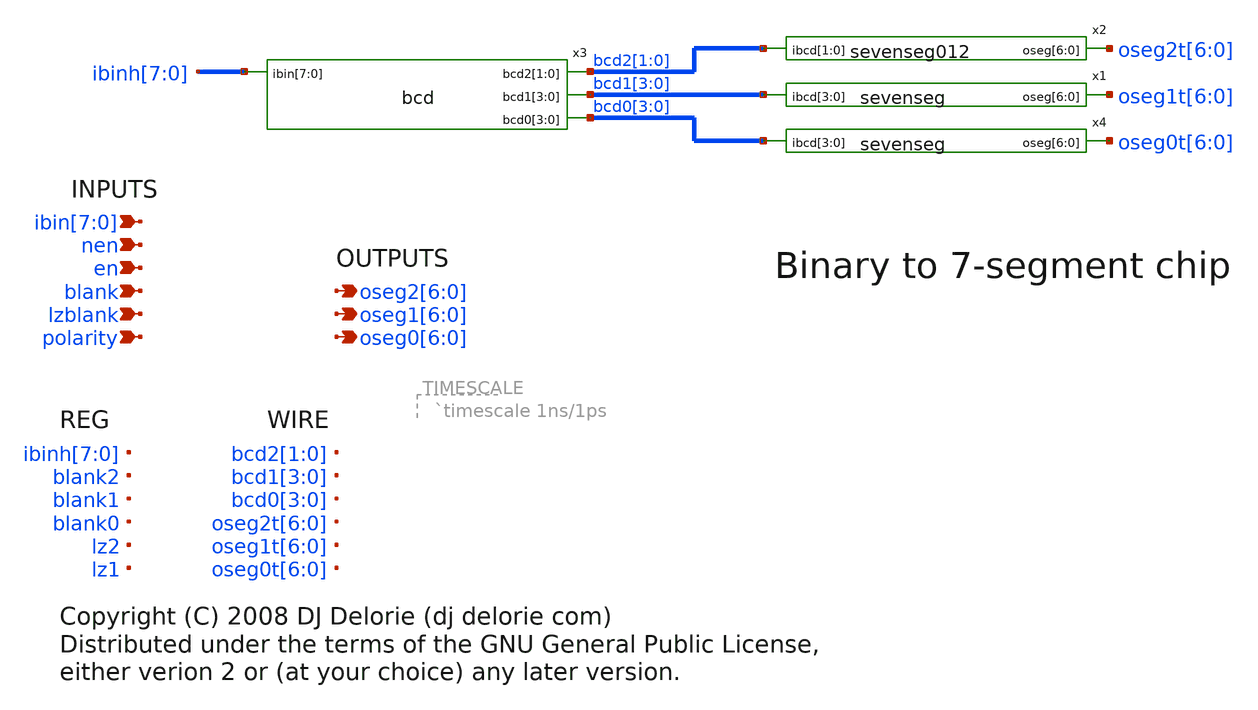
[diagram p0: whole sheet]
** sch_path: xschem-src/xschem_library/binto7seg/top.sch
* Copyright (C) 1998-2026 Stefan Frederik Schippers
* This program is free software; you can redistribute it and/or modify
* it under the terms of the GNU General Public License as published by
* the Free Software Foundation; either version 2 of the License, or
* (at your option) any later version.
* This program is distributed in the hope that it will be useful,
* but WITHOUT ANY WARRANTY; without even the implied warranty of
* MERCHANTABILITY or FITNESS FOR A PARTICULAR PURPOSE.  See the
* GNU General Public License for more details.
* You should have received a copy of the GNU General Public License
* along with this program; if not, write to the Free Software
* xschem-src/xschem_library/binto7seg/bcd.sch:
* C {code.sym} 260 -380 0 0 {name=CODE value="// Copyright (C) 2008 DJ Delorie <dj delorie com>
**.subckt top nen en blank polarity lzblank
*+ ibin[7],ibin[6],ibin[5],ibin[4],ibin[3],ibin[2],ibin[1],ibin[0] oseg2[6],oseg2[5],oseg2[4],oseg2[3],oseg2[2],oseg2[1],oseg2[0]
*+ oseg1[6],oseg1[5],oseg1[4],oseg1[3],oseg1[2],oseg1[1],oseg1[0] oseg0[6],oseg0[5],oseg0[4],oseg0[3],oseg0[2],oseg0[1],oseg0[0]
*.ipin nen
*.ipin en
*.ipin blank
*.ipin polarity
*.ipin lzblank
*.ipin ibin[7],ibin[6],ibin[5],ibin[4],ibin[3],ibin[2],ibin[1],ibin[0]
*.opin oseg2[6],oseg2[5],oseg2[4],oseg2[3],oseg2[2],oseg2[1],oseg2[0]
*.opin oseg1[6],oseg1[5],oseg1[4],oseg1[3],oseg1[2],oseg1[1],oseg1[0]
*.opin oseg0[6],oseg0[5],oseg0[4],oseg0[3],oseg0[2],oseg0[1],oseg0[0]
x1 oseg1t[6] oseg1t[5] oseg1t[4] oseg1t[3] oseg1t[2] oseg1t[1] oseg1t[0] bcd1[3] bcd1[2] bcd1[1]
+ bcd1[0] sevenseg
x2 oseg2t[6] oseg2t[5] oseg2t[4] oseg2t[3] oseg2t[2] oseg2t[1] oseg2t[0] bcd2[1] bcd2[0] sevenseg012
x3 bcd2[1] bcd2[0] ibinh[7] ibinh[6] ibinh[5] ibinh[4] ibinh[3] ibinh[2] ibinh[1] ibinh[0] bcd1[3]
+ bcd1[2] bcd1[1] bcd1[0] bcd0[3] bcd0[2] bcd0[1] bcd0[0] bcd
x4 oseg0t[6] oseg0t[5] oseg0t[4] oseg0t[3] oseg0t[2] oseg0t[1] oseg0t[0] bcd0[3] bcd0[2] bcd0[1]
+ bcd0[0] sevenseg
**** begin user architecture code

// Copyright (C) 2008 DJ Delorie <dj delorie com>
// Distributed under the terms of the GNU General Public License,
// either verion 2 or (at your choice) any later version.

always @ (ibin, nen, en)
begin
  if (en & ~ nen)
    ibinh = ibin;
  else
    ibinh = ibinh;
end


always @ (bcd2, bcd1)
begin
  lz2 = (bcd2 == 0) ? 1 : 0;
  lz1 = (bcd1 == 0) ? lz2 : 0;
end

always @ (lz2, lz1, lzblank, blank)
begin
  blank2 = (lzblank & lz2) | blank;
  blank1 = (lzblank & lz1) | blank;
  blank0 = blank;
end

always @ (oseg2t, polarity, blank2)
begin
  if (blank2)
    oseg2 = 7'bZ;
  else if (polarity)
    oseg2 = ~ oseg2t;
  else
    oseg2 = oseg2t;
end

always @ (oseg1t, polarity, blank1, blank2)
begin
  if (blank1)
    oseg1 = 7'bZ;
  else if (polarity)
    oseg1 = ~ oseg1t;
  else
    oseg1 = oseg1t;
end

always @ (oseg0t, polarity, blank0)
begin
  if (blank0)
    oseg0 = 7'bZ;
  else if (polarity)
    oseg0 = ~ oseg0t;
  else
    oseg0 = oseg0t;
end




reg [7:0] iibin;
reg ien;
reg inen;
reg iblank;
reg ilzblank;
reg ipolarity;

initial begin
  $dumpfile("dumpfile.vcd");
  $dumpvars(0, top);
end

task binpattern;
begin
  iibin = 0;
  #100;
  iibin = 1;
  #100;
  iibin = 2;
  #100;
  iibin = 234;
  #100;
  iibin = 255;
  #100;
  iibin = 188;
  #100;
  iibin = 222;
  #100;
end endtask

initial begin
  ien = 1;
  inen = 0;
  iblank = 0;
  ilzblank = 0;
  ipolarity = 0;
  binpattern;
  ilzblank = 1; // blank leading zeros
  binpattern;
end

assign en = ien;
assign nen = inen;
assign ibin = iibin;
assign blank = iblank;
assign lzblank = ilzblank;
assign polarity = ipolarity;


**** end user architecture code
**.ends

* expanding   symbol:  sevenseg.sym # of pins=2
** sym_path: xschem-src/xschem_library/binto7seg/sevenseg.sym
** sch_path: xschem-src/xschem_library/binto7seg/sevenseg.sch
.subckt sevenseg oseg[6] oseg[5] oseg[4] oseg[3] oseg[2] oseg[1] oseg[0] ibcd[3] ibcd[2] ibcd[1] ibcd[0]
*.ipin ibcd[3],ibcd[2],ibcd[1],ibcd[0]
*.opin oseg[6],oseg[5],oseg[4],oseg[3],oseg[2],oseg[1],oseg[0]
**** begin user architecture code

// Copyright (C) 2008 DJ Delorie <dj delorie com>
// Distributed under the terms of the GNU General Public License,
// either verion 2 or (at your choice) any later version.

always @ (ibcd)
begin
  case (ibcd)  // abcdefg
    0 : oseg = 7'b1111110;
    1 : oseg = 7'b0110000;
    2 : oseg = 7'b1101101;
    3 : oseg = 7'b1111001;
    4 : oseg = 7'b0110011;
    5 : oseg = 7'b1011011;
    6 : oseg = 7'b1011111;
    7 : oseg = 7'b1110000;
    8 : oseg = 7'b1111111;
    9 : oseg = 7'b1111011;
    default : oseg = 0;
  endcase
end



**** end user architecture code
.ends


* expanding   symbol:  sevenseg012.sym # of pins=2
** sym_path: xschem-src/xschem_library/binto7seg/sevenseg012.sym
** sch_path: xschem-src/xschem_library/binto7seg/sevenseg012.sch
.subckt sevenseg012 oseg[6] oseg[5] oseg[4] oseg[3] oseg[2] oseg[1] oseg[0] ibcd[1] ibcd[0]
*.ipin ibcd[1],ibcd[0]
*.opin oseg[6],oseg[5],oseg[4],oseg[3],oseg[2],oseg[1],oseg[0]
**** begin user architecture code

// Copyright (C) 2008 DJ Delorie <dj delorie com>
// Distributed under the terms of the GNU General Public License,
// either verion 2 or (at your choice) any later version.

always @ (ibcd)
begin
  case (ibcd)  // abcdefg
    0 : oseg = 7'b1111110;
    1 : oseg = 7'b0110000;
    2 : oseg = 7'b1101101;
    default : oseg = 0;
  endcase
end


**** end user architecture code
.ends


* expanding   symbol:  bcd.sym # of pins=4
** sym_path: xschem-src/xschem_library/binto7seg/bcd.sym
** sch_path: xschem-src/xschem_library/binto7seg/bcd.sch
.subckt bcd bcd2[1] bcd2[0] ibin[7] ibin[6] ibin[5] ibin[4] ibin[3] ibin[2] ibin[1] ibin[0] bcd1[3]
+ bcd1[2] bcd1[1] bcd1[0] bcd0[3] bcd0[2] bcd0[1] bcd0[0]
*.ipin ibin[7],ibin[6],ibin[5],ibin[4],ibin[3],ibin[2],ibin[1],ibin[0]
*.opin bcd2[1],bcd2[0]
*.opin bcd1[3],bcd1[2],bcd1[1],bcd1[0]
*.opin bcd0[3],bcd0[2],bcd0[1],bcd0[0]
**** begin user architecture code

// Copyright (C) 2008 DJ Delorie <dj delorie com>
// Distributed under the terms of the GNU General Public License,
// either verion 2 or (at your choice) any later version.

always @ (ibin)
begin

  case (ibin)
    0 : begin bcd2 <= 2'b00; bcd1 <= 4'b0000; bcd0 <= 4'b0000; end
    1 : begin bcd2 <= 2'b00; bcd1 <= 4'b0000; bcd0 <= 4'b0001; end
    2 : begin bcd2 <= 2'b00; bcd1 <= 4'b0000; bcd0 <= 4'b0010; end
    3 : begin bcd2 <= 2'b00; bcd1 <= 4'b0000; bcd0 <= 4'b0011; end
    4 : begin bcd2 <= 2'b00; bcd1 <= 4'b0000; bcd0 <= 4'b0100; end
    5 : begin bcd2 <= 2'b00; bcd1 <= 4'b0000; bcd0 <= 4'b0101; end
    6 : begin bcd2 <= 2'b00; bcd1 <= 4'b0000; bcd0 <= 4'b0110; end
    7 : begin bcd2 <= 2'b00; bcd1 <= 4'b0000; bcd0 <= 4'b0111; end
    8 : begin bcd2 <= 2'b00; bcd1 <= 4'b0000; bcd0 <= 4'b1000; end
    9 : begin bcd2 <= 2'b00; bcd1 <= 4'b0000; bcd0 <= 4'b1001; end
    10 : begin bcd2 <= 2'b00; bcd1 <= 4'b0001; bcd0 <= 4'b0000; end
    11 : begin bcd2 <= 2'b00; bcd1 <= 4'b0001; bcd0 <= 4'b0001; end
    12 : begin bcd2 <= 2'b00; bcd1 <= 4'b0001; bcd0 <= 4'b0010; end
    13 : begin bcd2 <= 2'b00; bcd1 <= 4'b0001; bcd0 <= 4'b0011; end
    14 : begin bcd2 <= 2'b00; bcd1 <= 4'b0001; bcd0 <= 4'b0100; end
    15 : begin bcd2 <= 2'b00; bcd1 <= 4'b0001; bcd0 <= 4'b0101; end
    16 : begin bcd2 <= 2'b00; bcd1 <= 4'b0001; bcd0 <= 4'b0110; end
    17 : begin bcd2 <= 2'b00; bcd1 <= 4'b0001; bcd0 <= 4'b0111; end
    18 : begin bcd2 <= 2'b00; bcd1 <= 4'b0001; bcd0 <= 4'b1000; end
    19 : begin bcd2 <= 2'b00; bcd1 <= 4'b0001; bcd0 <= 4'b1001; end
    20 : begin bcd2 <= 2'b00; bcd1 <= 4'b0010; bcd0 <= 4'b0000; end
    21 : begin bcd2 <= 2'b00; bcd1 <= 4'b0010; bcd0 <= 4'b0001; end
    22 : begin bcd2 <= 2'b00; bcd1 <= 4'b0010; bcd0 <= 4'b0010; end
    23 : begin bcd2 <= 2'b00; bcd1 <= 4'b0010; bcd0 <= 4'b0011; end
    24 : begin bcd2 <= 2'b00; bcd1 <= 4'b0010; bcd0 <= 4'b0100; end
    25 : begin bcd2 <= 2'b00; bcd1 <= 4'b0010; bcd0 <= 4'b0101; end
    26 : begin bcd2 <= 2'b00; bcd1 <= 4'b0010; bcd0 <= 4'b0110; end
    27 : begin bcd2 <= 2'b00; bcd1 <= 4'b0010; bcd0 <= 4'b0111; end
    28 : begin bcd2 <= 2'b00; bcd1 <= 4'b0010; bcd0 <= 4'b1000; end
    29 : begin bcd2 <= 2'b00; bcd1 <= 4'b0010; bcd0 <= 4'b1001; end
    30 : begin bcd2 <= 2'b00; bcd1 <= 4'b0011; bcd0 <= 4'b0000; end
    31 : begin bcd2 <= 2'b00; bcd1 <= 4'b0011; bcd0 <= 4'b0001; end
    32 : begin bcd2 <= 2'b00; bcd1 <= 4'b0011; bcd0 <= 4'b0010; end
    33 : begin bcd2 <= 2'b00; bcd1 <= 4'b0011; bcd0 <= 4'b0011; end
    34 : begin bcd2 <= 2'b00; bcd1 <= 4'b0011; bcd0 <= 4'b0100; end
    35 : begin bcd2 <= 2'b00; bcd1 <= 4'b0011; bcd0 <= 4'b0101; end
    36 : begin bcd2 <= 2'b00; bcd1 <= 4'b0011; bcd0 <= 4'b0110; end
    37 : begin bcd2 <= 2'b00; bcd1 <= 4'b0011; bcd0 <= 4'b0111; end
    38 : begin bcd2 <= 2'b00; bcd1 <= 4'b0011; bcd0 <= 4'b1000; end
    39 : begin bcd2 <= 2'b00; bcd1 <= 4'b0011; bcd0 <= 4'b1001; end
    40 : begin bcd2 <= 2'b00; bcd1 <= 4'b0100; bcd0 <= 4'b0000; end
    41 : begin bcd2 <= 2'b00; bcd1 <= 4'b0100; bcd0 <= 4'b0001; end
    42 : begin bcd2 <= 2'b00; bcd1 <= 4'b0100; bcd0 <= 4'b0010; end
    43 : begin bcd2 <= 2'b00; bcd1 <= 4'b0100; bcd0 <= 4'b0011; end
    44 : begin bcd2 <= 2'b00; bcd1 <= 4'b0100; bcd0 <= 4'b0100; end
    45 : begin bcd2 <= 2'b00; bcd1 <= 4'b0100; bcd0 <= 4'b0101; end
    46 : begin bcd2 <= 2'b00; bcd1 <= 4'b0100; bcd0 <= 4'b0110; end
    47 : begin bcd2 <= 2'b00; bcd1 <= 4'b0100; bcd0 <= 4'b0111; end
    48 : begin bcd2 <= 2'b00; bcd1 <= 4'b0100; bcd0 <= 4'b1000; end
    49 : begin bcd2 <= 2'b00; bcd1 <= 4'b0100; bcd0 <= 4'b1001; end
    50 : begin bcd2 <= 2'b00; bcd1 <= 4'b0101; bcd0 <= 4'b0000; end
    51 : begin bcd2 <= 2'b00; bcd1 <= 4'b0101; bcd0 <= 4'b0001; end
    52 : begin bcd2 <= 2'b00; bcd1 <= 4'b0101; bcd0 <= 4'b0010; end
    53 : begin bcd2 <= 2'b00; bcd1 <= 4'b0101; bcd0 <= 4'b0011; end
    54 : begin bcd2 <= 2'b00; bcd1 <= 4'b0101; bcd0 <= 4'b0100; end
    55 : begin bcd2 <= 2'b00; bcd1 <= 4'b0101; bcd0 <= 4'b0101; end
    56 : begin bcd2 <= 2'b00; bcd1 <= 4'b0101; bcd0 <= 4'b0110; end
    57 : begin bcd2 <= 2'b00; bcd1 <= 4'b0101; bcd0 <= 4'b0111; end
    58 : begin bcd2 <= 2'b00; bcd1 <= 4'b0101; bcd0 <= 4'b1000; end
    59 : begin bcd2 <= 2'b00; bcd1 <= 4'b0101; bcd0 <= 4'b1001; end
    60 : begin bcd2 <= 2'b00; bcd1 <= 4'b0110; bcd0 <= 4'b0000; end
    61 : begin bcd2 <= 2'b00; bcd1 <= 4'b0110; bcd0 <= 4'b0001; end
    62 : begin bcd2 <= 2'b00; bcd1 <= 4'b0110; bcd0 <= 4'b0010; end
    63 : begin bcd2 <= 2'b00; bcd1 <= 4'b0110; bcd0 <= 4'b0011; end
    64 : begin bcd2 <= 2'b00; bcd1 <= 4'b0110; bcd0 <= 4'b0100; end
    65 : begin bcd2 <= 2'b00; bcd1 <= 4'b0110; bcd0 <= 4'b0101; end
    66 : begin bcd2 <= 2'b00; bcd1 <= 4'b0110; bcd0 <= 4'b0110; end
    67 : begin bcd2 <= 2'b00; bcd1 <= 4'b0110; bcd0 <= 4'b0111; end
    68 : begin bcd2 <= 2'b00; bcd1 <= 4'b0110; bcd0 <= 4'b1000; end
    69 : begin bcd2 <= 2'b00; bcd1 <= 4'b0110; bcd0 <= 4'b1001; end
    70 : begin bcd2 <= 2'b00; bcd1 <= 4'b0111; bcd0 <= 4'b0000; end
    71 : begin bcd2 <= 2'b00; bcd1 <= 4'b0111; bcd0 <= 4'b0001; end
    72 : begin bcd2 <= 2'b00; bcd1 <= 4'b0111; bcd0 <= 4'b0010; end
    73 : begin bcd2 <= 2'b00; bcd1 <= 4'b0111; bcd0 <= 4'b0011; end
    74 : begin bcd2 <= 2'b00; bcd1 <= 4'b0111; bcd0 <= 4'b0100; end
    75 : begin bcd2 <= 2'b00; bcd1 <= 4'b0111; bcd0 <= 4'b0101; end
    76 : begin bcd2 <= 2'b00; bcd1 <= 4'b0111; bcd0 <= 4'b0110; end
    77 : begin bcd2 <= 2'b00; bcd1 <= 4'b0111; bcd0 <= 4'b0111; end
    78 : begin bcd2 <= 2'b00; bcd1 <= 4'b0111; bcd0 <= 4'b1000; end
    79 : begin bcd2 <= 2'b00; bcd1 <= 4'b0111; bcd0 <= 4'b1001; end
    80 : begin bcd2 <= 2'b00; bcd1 <= 4'b1000; bcd0 <= 4'b0000; end
    81 : begin bcd2 <= 2'b00; bcd1 <= 4'b1000; bcd0 <= 4'b0001; end
    82 : begin bcd2 <= 2'b00; bcd1 <= 4'b1000; bcd0 <= 4'b0010; end
    83 : begin bcd2 <= 2'b00; bcd1 <= 4'b1000; bcd0 <= 4'b0011; end
    84 : begin bcd2 <= 2'b00; bcd1 <= 4'b1000; bcd0 <= 4'b0100; end
    85 : begin bcd2 <= 2'b00; bcd1 <= 4'b1000; bcd0 <= 4'b0101; end
    86 : begin bcd2 <= 2'b00; bcd1 <= 4'b1000; bcd0 <= 4'b0110; end
    87 : begin bcd2 <= 2'b00; bcd1 <= 4'b1000; bcd0 <= 4'b0111; end
    88 : begin bcd2 <= 2'b00; bcd1 <= 4'b1000; bcd0 <= 4'b1000; end
    89 : begin bcd2 <= 2'b00; bcd1 <= 4'b1000; bcd0 <= 4'b1001; end
    90 : begin bcd2 <= 2'b00; bcd1 <= 4'b1001; bcd0 <= 4'b0000; end
    91 : begin bcd2 <= 2'b00; bcd1 <= 4'b1001; bcd0 <= 4'b0001; end
    92 : begin bcd2 <= 2'b00; bcd1 <= 4'b1001; bcd0 <= 4'b0010; end
    93 : begin bcd2 <= 2'b00; bcd1 <= 4'b1001; bcd0 <= 4'b0011; end
    94 : begin bcd2 <= 2'b00; bcd1 <= 4'b1001; bcd0 <= 4'b0100; end
    95 : begin bcd2 <= 2'b00; bcd1 <= 4'b1001; bcd0 <= 4'b0101; end
    96 : begin bcd2 <= 2'b00; bcd1 <= 4'b1001; bcd0 <= 4'b0110; end
    97 : begin bcd2 <= 2'b00; bcd1 <= 4'b1001; bcd0 <= 4'b0111; end
    98 : begin bcd2 <= 2'b00; bcd1 <= 4'b1001; bcd0 <= 4'b1000; end
    99 : begin bcd2 <= 2'b00; bcd1 <= 4'b1001; bcd0 <= 4'b1001; end
    100 : begin bcd2 <= 2'b01; bcd1 <= 4'b0000; bcd0 <= 4'b0000; end
    101 : begin bcd2 <= 2'b01; bcd1 <= 4'b0000; bcd0 <= 4'b0001; end
    102 : begin bcd2 <= 2'b01; bcd1 <= 4'b0000; bcd0 <= 4'b0010; end
    103 : begin bcd2 <= 2'b01; bcd1 <= 4'b0000; bcd0 <= 4'b0011; end
    104 : begin bcd2 <= 2'b01; bcd1 <= 4'b0000; bcd0 <= 4'b0100; end
    105 : begin bcd2 <= 2'b01; bcd1 <= 4'b0000; bcd0 <= 4'b0101; end
    106 : begin bcd2 <= 2'b01; bcd1 <= 4'b0000; bcd0 <= 4'b0110; end
    107 : begin bcd2 <= 2'b01; bcd1 <= 4'b0000; bcd0 <= 4'b0111; end
    108 : begin bcd2 <= 2'b01; bcd1 <= 4'b0000; bcd0 <= 4'b1000; end
    109 : begin bcd2 <= 2'b01; bcd1 <= 4'b0000; bcd0 <= 4'b1001; end
    110 : begin bcd2 <= 2'b01; bcd1 <= 4'b0001; bcd0 <= 4'b0000; end
    111 : begin bcd2 <= 2'b01; bcd1 <= 4'b0001; bcd0 <= 4'b0001; end
    112 : begin bcd2 <= 2'b01; bcd1 <= 4'b0001; bcd0 <= 4'b0010; end
    113 : begin bcd2 <= 2'b01; bcd1 <= 4'b0001; bcd0 <= 4'b0011; end
    114 : begin bcd2 <= 2'b01; bcd1 <= 4'b0001; bcd0 <= 4'b0100; end
    115 : begin bcd2 <= 2'b01; bcd1 <= 4'b0001; bcd0 <= 4'b0101; end
    116 : begin bcd2 <= 2'b01; bcd1 <= 4'b0001; bcd0 <= 4'b0110; end
    117 : begin bcd2 <= 2'b01; bcd1 <= 4'b0001; bcd0 <= 4'b0111; end
    118 : begin bcd2 <= 2'b01; bcd1 <= 4'b0001; bcd0 <= 4'b1000; end
    119 : begin bcd2 <= 2'b01; bcd1 <= 4'b0001; bcd0 <= 4'b1001; end
    120 : begin bcd2 <= 2'b01; bcd1 <= 4'b0010; bcd0 <= 4'b0000; end
    121 : begin bcd2 <= 2'b01; bcd1 <= 4'b0010; bcd0 <= 4'b0001; end
    122 : begin bcd2 <= 2'b01; bcd1 <= 4'b0010; bcd0 <= 4'b0010; end
    123 : begin bcd2 <= 2'b01; bcd1 <= 4'b0010; bcd0 <= 4'b0011; end
    124 : begin bcd2 <= 2'b01; bcd1 <= 4'b0010; bcd0 <= 4'b0100; end
    125 : begin bcd2 <= 2'b01; bcd1 <= 4'b0010; bcd0 <= 4'b0101; end
    126 : begin bcd2 <= 2'b01; bcd1 <= 4'b0010; bcd0 <= 4'b0110; end
    127 : begin bcd2 <= 2'b01; bcd1 <= 4'b0010; bcd0 <= 4'b0111; end
    128 : begin bcd2 <= 2'b01; bcd1 <= 4'b0010; bcd0 <= 4'b1000; end
    129 : begin bcd2 <= 2'b01; bcd1 <= 4'b0010; bcd0 <= 4'b1001; end
    130 : begin bcd2 <= 2'b01; bcd1 <= 4'b0011; bcd0 <= 4'b0000; end
    131 : begin bcd2 <= 2'b01; bcd1 <= 4'b0011; bcd0 <= 4'b0001; end
    132 : begin bcd2 <= 2'b01; bcd1 <= 4'b0011; bcd0 <= 4'b0010; end
    133 : begin bcd2 <= 2'b01; bcd1 <= 4'b0011; bcd0 <= 4'b0011; end
    134 : begin bcd2 <= 2'b01; bcd1 <= 4'b0011; bcd0 <= 4'b0100; end
    135 : begin bcd2 <= 2'b01; bcd1 <= 4'b0011; bcd0 <= 4'b0101; end
    136 : begin bcd2 <= 2'b01; bcd1 <= 4'b0011; bcd0 <= 4'b0110; end
    137 : begin bcd2 <= 2'b01; bcd1 <= 4'b0011; bcd0 <= 4'b0111; end
    138 : begin bcd2 <= 2'b01; bcd1 <= 4'b0011; bcd0 <= 4'b1000; end
    139 : begin bcd2 <= 2'b01; bcd1 <= 4'b0011; bcd0 <= 4'b1001; end
    140 : begin bcd2 <= 2'b01; bcd1 <= 4'b0100; bcd0 <= 4'b0000; end
    141 : begin bcd2 <= 2'b01; bcd1 <= 4'b0100; bcd0 <= 4'b0001; end
    142 : begin bcd2 <= 2'b01; bcd1 <= 4'b0100; bcd0 <= 4'b0010; end
    143 : begin bcd2 <= 2'b01; bcd1 <= 4'b0100; bcd0 <= 4'b0011; end
    144 : begin bcd2 <= 2'b01; bcd1 <= 4'b0100; bcd0 <= 4'b0100; end
    145 : begin bcd2 <= 2'b01; bcd1 <= 4'b0100; bcd0 <= 4'b0101; end
    146 : begin bcd2 <= 2'b01; bcd1 <= 4'b0100; bcd0 <= 4'b0110; end
    147 : begin bcd2 <= 2'b01; bcd1 <= 4'b0100; bcd0 <= 4'b0111; end
    148 : begin bcd2 <= 2'b01; bcd1 <= 4'b0100; bcd0 <= 4'b1000; end
    149 : begin bcd2 <= 2'b01; bcd1 <= 4'b0100; bcd0 <= 4'b1001; end
    150 : begin bcd2 <= 2'b01; bcd1 <= 4'b0101; bcd0 <= 4'b0000; end
    151 : begin bcd2 <= 2'b01; bcd1 <= 4'b0101; bcd0 <= 4'b0001; end
    152 : begin bcd2 <= 2'b01; bcd1 <= 4'b0101; bcd0 <= 4'b0010; end
    153 : begin bcd2 <= 2'b01; bcd1 <= 4'b0101; bcd0 <= 4'b0011; end
    154 : begin bcd2 <= 2'b01; bcd1 <= 4'b0101; bcd0 <= 4'b0100; end
    155 : begin bcd2 <= 2'b01; bcd1 <= 4'b0101; bcd0 <= 4'b0101; end
    156 : begin bcd2 <= 2'b01; bcd1 <= 4'b0101; bcd0 <= 4'b0110; end
    157 : begin bcd2 <= 2'b01; bcd1 <= 4'b0101; bcd0 <= 4'b0111; end
    158 : begin bcd2 <= 2'b01; bcd1 <= 4'b0101; bcd0 <= 4'b1000; end
    159 : begin bcd2 <= 2'b01; bcd1 <= 4'b0101; bcd0 <= 4'b1001; end
    160 : begin bcd2 <= 2'b01; bcd1 <= 4'b0110; bcd0 <= 4'b0000; end
    161 : begin bcd2 <= 2'b01; bcd1 <= 4'b0110; bcd0 <= 4'b0001; end
    162 : begin bcd2 <= 2'b01; bcd1 <= 4'b0110; bcd0 <= 4'b0010; end
    163 : begin bcd2 <= 2'b01; bcd1 <= 4'b0110; bcd0 <= 4'b0011; end
    164 : begin bcd2 <= 2'b01; bcd1 <= 4'b0110; bcd0 <= 4'b0100; end
    165 : begin bcd2 <= 2'b01; bcd1 <= 4'b0110; bcd0 <= 4'b0101; end
    166 : begin bcd2 <= 2'b01; bcd1 <= 4'b0110; bcd0 <= 4'b0110; end
    167 : begin bcd2 <= 2'b01; bcd1 <= 4'b0110; bcd0 <= 4'b0111; end
    168 : begin bcd2 <= 2'b01; bcd1 <= 4'b0110; bcd0 <= 4'b1000; end
    169 : begin bcd2 <= 2'b01; bcd1 <= 4'b0110; bcd0 <= 4'b1001; end
    170 : begin bcd2 <= 2'b01; bcd1 <= 4'b0111; bcd0 <= 4'b0000; end
    171 : begin bcd2 <= 2'b01; bcd1 <= 4'b0111; bcd0 <= 4'b0001; end
    172 : begin bcd2 <= 2'b01; bcd1 <= 4'b0111; bcd0 <= 4'b0010; end
    173 : begin bcd2 <= 2'b01; bcd1 <= 4'b0111; bcd0 <= 4'b0011; end
    174 : begin bcd2 <= 2'b01; bcd1 <= 4'b0111; bcd0 <= 4'b0100; end
    175 : begin bcd2 <= 2'b01; bcd1 <= 4'b0111; bcd0 <= 4'b0101; end
    176 : begin bcd2 <= 2'b01; bcd1 <= 4'b0111; bcd0 <= 4'b0110; end
    177 : begin bcd2 <= 2'b01; bcd1 <= 4'b0111; bcd0 <= 4'b0111; end
    178 : begin bcd2 <= 2'b01; bcd1 <= 4'b0111; bcd0 <= 4'b1000; end
    179 : begin bcd2 <= 2'b01; bcd1 <= 4'b0111; bcd0 <= 4'b1001; end
    180 : begin bcd2 <= 2'b01; bcd1 <= 4'b1000; bcd0 <= 4'b0000; end
    181 : begin bcd2 <= 2'b01; bcd1 <= 4'b1000; bcd0 <= 4'b0001; end
    182 : begin bcd2 <= 2'b01; bcd1 <= 4'b1000; bcd0 <= 4'b0010; end
    183 : begin bcd2 <= 2'b01; bcd1 <= 4'b1000; bcd0 <= 4'b0011; end
    184 : begin bcd2 <= 2'b01; bcd1 <= 4'b1000; bcd0 <= 4'b0100; end
    185 : begin bcd2 <= 2'b01; bcd1 <= 4'b1000; bcd0 <= 4'b0101; end
    186 : begin bcd2 <= 2'b01; bcd1 <= 4'b1000; bcd0 <= 4'b0110; end
    187 : begin bcd2 <= 2'b01; bcd1 <= 4'b1000; bcd0 <= 4'b0111; end
    188 : begin bcd2 <= 2'b01; bcd1 <= 4'b1000; bcd0 <= 4'b1000; end
    189 : begin bcd2 <= 2'b01; bcd1 <= 4'b1000; bcd0 <= 4'b1001; end
    190 : begin bcd2 <= 2'b01; bcd1 <= 4'b1001; bcd0 <= 4'b0000; end
    191 : begin bcd2 <= 2'b01; bcd1 <= 4'b1001; bcd0 <= 4'b0001; end
    192 : begin bcd2 <= 2'b01; bcd1 <= 4'b1001; bcd0 <= 4'b0010; end
    193 : begin bcd2 <= 2'b01; bcd1 <= 4'b1001; bcd0 <= 4'b0011; end
    194 : begin bcd2 <= 2'b01; bcd1 <= 4'b1001; bcd0 <= 4'b0100; end
    195 : begin bcd2 <= 2'b01; bcd1 <= 4'b1001; bcd0 <= 4'b0101; end
    196 : begin bcd2 <= 2'b01; bcd1 <= 4'b1001; bcd0 <= 4'b0110; end
    197 : begin bcd2 <= 2'b01; bcd1 <= 4'b1001; bcd0 <= 4'b0111; end
    198 : begin bcd2 <= 2'b01; bcd1 <= 4'b1001; bcd0 <= 4'b1000; end
    199 : begin bcd2 <= 2'b01; bcd1 <= 4'b1001; bcd0 <= 4'b1001; end
    200 : begin bcd2 <= 2'b10; bcd1 <= 4'b0000; bcd0 <= 4'b0000; end
    201 : begin bcd2 <= 2'b10; bcd1 <= 4'b0000; bcd0 <= 4'b0001; end
    202 : begin bcd2 <= 2'b10; bcd1 <= 4'b0000; bcd0 <= 4'b0010; end
    203 : begin bcd2 <= 2'b10; bcd1 <= 4'b0000; bcd0 <= 4'b0011; end
    204 : begin bcd2 <= 2'b10; bcd1 <= 4'b0000; bcd0 <= 4'b0100; end
    205 : begin bcd2 <= 2'b10; bcd1 <= 4'b0000; bcd0 <= 4'b0101; end
    206 : begin bcd2 <= 2'b10; bcd1 <= 4'b0000; bcd0 <= 4'b0110; end
    207 : begin bcd2 <= 2'b10; bcd1 <= 4'b0000; bcd0 <= 4'b0111; end
    208 : begin bcd2 <= 2'b10; bcd1 <= 4'b0000; bcd0 <= 4'b1000; end
    209 : begin bcd2 <= 2'b10; bcd1 <= 4'b0000; bcd0 <= 4'b1001; end
    210 : begin bcd2 <= 2'b10; bcd1 <= 4'b0001; bcd0 <= 4'b0000; end
    211 : begin bcd2 <= 2'b10; bcd1 <= 4'b0001; bcd0 <= 4'b0001; end
    212 : begin bcd2 <= 2'b10; bcd1 <= 4'b0001; bcd0 <= 4'b0010; end
    213 : begin bcd2 <= 2'b10; bcd1 <= 4'b0001; bcd0 <= 4'b0011; end
    214 : begin bcd2 <= 2'b10; bcd1 <= 4'b0001; bcd0 <= 4'b0100; end
    215 : begin bcd2 <= 2'b10; bcd1 <= 4'b0001; bcd0 <= 4'b0101; end
    216 : begin bcd2 <= 2'b10; bcd1 <= 4'b0001; bcd0 <= 4'b0110; end
    217 : begin bcd2 <= 2'b10; bcd1 <= 4'b0001; bcd0 <= 4'b0111; end
    218 : begin bcd2 <= 2'b10; bcd1 <= 4'b0001; bcd0 <= 4'b1000; end
    219 : begin bcd2 <= 2'b10; bcd1 <= 4'b0001; bcd0 <= 4'b1001; end
    220 : begin bcd2 <= 2'b10; bcd1 <= 4'b0010; bcd0 <= 4'b0000; end
    221 : begin bcd2 <= 2'b10; bcd1 <= 4'b0010; bcd0 <= 4'b0001; end
    222 : begin bcd2 <= 2'b10; bcd1 <= 4'b0010; bcd0 <= 4'b0010; end
    223 : begin bcd2 <= 2'b10; bcd1 <= 4'b0010; bcd0 <= 4'b0011; end
    224 : begin bcd2 <= 2'b10; bcd1 <= 4'b0010; bcd0 <= 4'b0100; end
    225 : begin bcd2 <= 2'b10; bcd1 <= 4'b0010; bcd0 <= 4'b0101; end
    226 : begin bcd2 <= 2'b10; bcd1 <= 4'b0010; bcd0 <= 4'b0110; end
    227 : begin bcd2 <= 2'b10; bcd1 <= 4'b0010; bcd0 <= 4'b0111; end
    228 : begin bcd2 <= 2'b10; bcd1 <= 4'b0010; bcd0 <= 4'b1000; end
    229 : begin bcd2 <= 2'b10; bcd1 <= 4'b0010; bcd0 <= 4'b1001; end
    230 : begin bcd2 <= 2'b10; bcd1 <= 4'b0011; bcd0 <= 4'b0000; end
    231 : begin bcd2 <= 2'b10; bcd1 <= 4'b0011; bcd0 <= 4'b0001; end
    232 : begin bcd2 <= 2'b10; bcd1 <= 4'b0011; bcd0 <= 4'b0010; end
    233 : begin bcd2 <= 2'b10; bcd1 <= 4'b0011; bcd0 <= 4'b0011; end
    234 : begin bcd2 <= 2'b10; bcd1 <= 4'b0011; bcd0 <= 4'b0100; end
    235 : begin bcd2 <= 2'b10; bcd1 <= 4'b0011; bcd0 <= 4'b0101; end
    236 : begin bcd2 <= 2'b10; bcd1 <= 4'b0011; bcd0 <= 4'b0110; end
    237 : begin bcd2 <= 2'b10; bcd1 <= 4'b0011; bcd0 <= 4'b0111; end
    238 : begin bcd2 <= 2'b10; bcd1 <= 4'b0011; bcd0 <= 4'b1000; end
    239 : begin bcd2 <= 2'b10; bcd1 <= 4'b0011; bcd0 <= 4'b1001; end
    240 : begin bcd2 <= 2'b10; bcd1 <= 4'b0100; bcd0 <= 4'b0000; end
    241 : begin bcd2 <= 2'b10; bcd1 <= 4'b0100; bcd0 <= 4'b0001; end
    242 : begin bcd2 <= 2'b10; bcd1 <= 4'b0100; bcd0 <= 4'b0010; end
    243 : begin bcd2 <= 2'b10; bcd1 <= 4'b0100; bcd0 <= 4'b0011; end
    244 : begin bcd2 <= 2'b10; bcd1 <= 4'b0100; bcd0 <= 4'b0100; end
    245 : begin bcd2 <= 2'b10; bcd1 <= 4'b0100; bcd0 <= 4'b0101; end
    246 : begin bcd2 <= 2'b10; bcd1 <= 4'b0100; bcd0 <= 4'b0110; end
    247 : begin bcd2 <= 2'b10; bcd1 <= 4'b0100; bcd0 <= 4'b0111; end
    248 : begin bcd2 <= 2'b10; bcd1 <= 4'b0100; bcd0 <= 4'b1000; end
    249 : begin bcd2 <= 2'b10; bcd1 <= 4'b0100; bcd0 <= 4'b1001; end
    250 : begin bcd2 <= 2'b10; bcd1 <= 4'b0101; bcd0 <= 4'b0000; end
    251 : begin bcd2 <= 2'b10; bcd1 <= 4'b0101; bcd0 <= 4'b0001; end
    252 : begin bcd2 <= 2'b10; bcd1 <= 4'b0101; bcd0 <= 4'b0010; end
    253 : begin bcd2 <= 2'b10; bcd1 <= 4'b0101; bcd0 <= 4'b0011; end
    254 : begin bcd2 <= 2'b10; bcd1 <= 4'b0101; bcd0 <= 4'b0100; end
    255 : begin bcd2 <= 2'b10; bcd1 <= 4'b0101; bcd0 <= 4'b0101; end
  endcase
end


**** end user architecture code
.ends

.end
